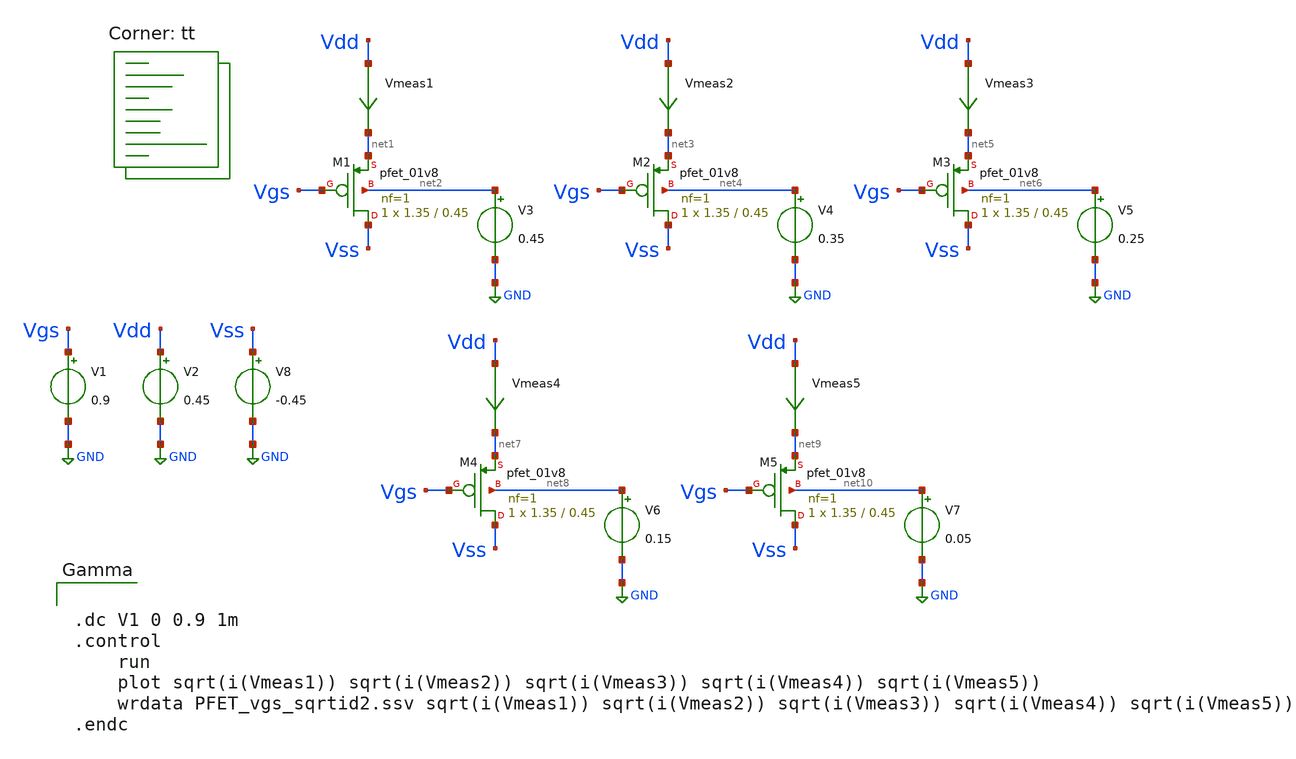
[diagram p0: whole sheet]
** sch_path: opamp_design/Parametros_cmos/PFET_param2.sch
**.subckt PFET_param2
Vmeas1 Vdd net1 0
.save i(vmeas1)
V2 Vdd GND 0.45
V1 Vgs GND 0.9
V3 net2 GND 0.45
Vmeas2 Vdd net3 0
.save i(vmeas2)
V4 net4 GND 0.35
Vmeas3 Vdd net5 0
.save i(vmeas3)
V5 net6 GND 0.25
Vmeas4 Vdd net7 0
.save i(vmeas4)
V6 net8 GND 0.15
Vmeas5 Vdd net9 0
.save i(vmeas5)
V7 net10 GND 0.05
V8 Vss GND -0.45
XM1 Vss Vgs net1 net2 sky130_fd_pr__pfet_01v8 L=0.45 W=1.35 nf=1 ad='int((nf+1)/2) * W/nf * 0.29' as='int((nf+2)/2) * W/nf * 0.29'
+ pd='2*int((nf+1)/2) * (W/nf + 0.29)' ps='2*int((nf+2)/2) * (W/nf + 0.29)' nrd='0.29 / W' nrs='0.29 / W'
+ sa=0 sb=0 sd=0 mult=1 m=1
XM2 Vss Vgs net3 net4 sky130_fd_pr__pfet_01v8 L=0.45 W=1.35 nf=1 ad='int((nf+1)/2) * W/nf * 0.29' as='int((nf+2)/2) * W/nf * 0.29'
+ pd='2*int((nf+1)/2) * (W/nf + 0.29)' ps='2*int((nf+2)/2) * (W/nf + 0.29)' nrd='0.29 / W' nrs='0.29 / W'
+ sa=0 sb=0 sd=0 mult=1 m=1
XM3 Vss Vgs net5 net6 sky130_fd_pr__pfet_01v8 L=0.45 W=1.35 nf=1 ad='int((nf+1)/2) * W/nf * 0.29' as='int((nf+2)/2) * W/nf * 0.29'
+ pd='2*int((nf+1)/2) * (W/nf + 0.29)' ps='2*int((nf+2)/2) * (W/nf + 0.29)' nrd='0.29 / W' nrs='0.29 / W'
+ sa=0 sb=0 sd=0 mult=1 m=1
XM4 Vss Vgs net7 net8 sky130_fd_pr__pfet_01v8 L=0.45 W=1.35 nf=1 ad='int((nf+1)/2) * W/nf * 0.29' as='int((nf+2)/2) * W/nf * 0.29'
+ pd='2*int((nf+1)/2) * (W/nf + 0.29)' ps='2*int((nf+2)/2) * (W/nf + 0.29)' nrd='0.29 / W' nrs='0.29 / W'
+ sa=0 sb=0 sd=0 mult=1 m=1
XM5 Vss Vgs net9 net10 sky130_fd_pr__pfet_01v8 L=0.45 W=1.35 nf=1 ad='int((nf+1)/2) * W/nf * 0.29' as='int((nf+2)/2) * W/nf * 0.29'
+ pd='2*int((nf+1)/2) * (W/nf + 0.29)' ps='2*int((nf+2)/2) * (W/nf + 0.29)' nrd='0.29 / W' nrs='0.29 / W'
+ sa=0 sb=0 sd=0 mult=1 m=1
**** begin user architecture code
.lib $::SKYWATER_MODELS/sky130.lib.spice tt


.dc V1 0 0.9 1m
.control
	run
	plot sqrt(i(Vmeas1)) sqrt(i(Vmeas2)) sqrt(i(Vmeas3)) sqrt(i(Vmeas4)) sqrt(i(Vmeas5))
	wrdata PFET_vgs_sqrtid2.ssv sqrt(i(Vmeas1)) sqrt(i(Vmeas2)) sqrt(i(Vmeas3)) sqrt(i(Vmeas4))
+ sqrt(i(Vmeas5))
.endc


**** end user architecture code
**.ends
.GLOBAL GND
.end
